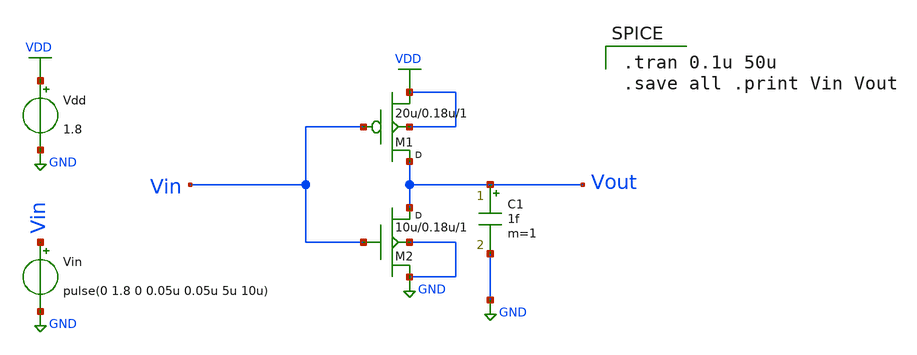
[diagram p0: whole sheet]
** sch_path: cells/inv/Inverter.sch
**.subckt Inverter
Vdd VDD GND 1.8
Vin Vin GND pulse(0 1.8 0 0.05u 0.05u 5u 10u)
M1 Vout Vin VDD VDD p1 w=20u l=0.18u m=1
M2 Vout Vin GND GND n1 w=10u l=0.18u m=1
C1 Vout GND 1f m=1
**** begin user architecture code


.model n1 nmos level=49 version=3.3.0
.model p1 pmos level=49 version=3.3.0


.tran 0.1u 50u
.save all .print Vin Vout

**** end user architecture code
**.ends
.GLOBAL VDD
.GLOBAL GND
.end
